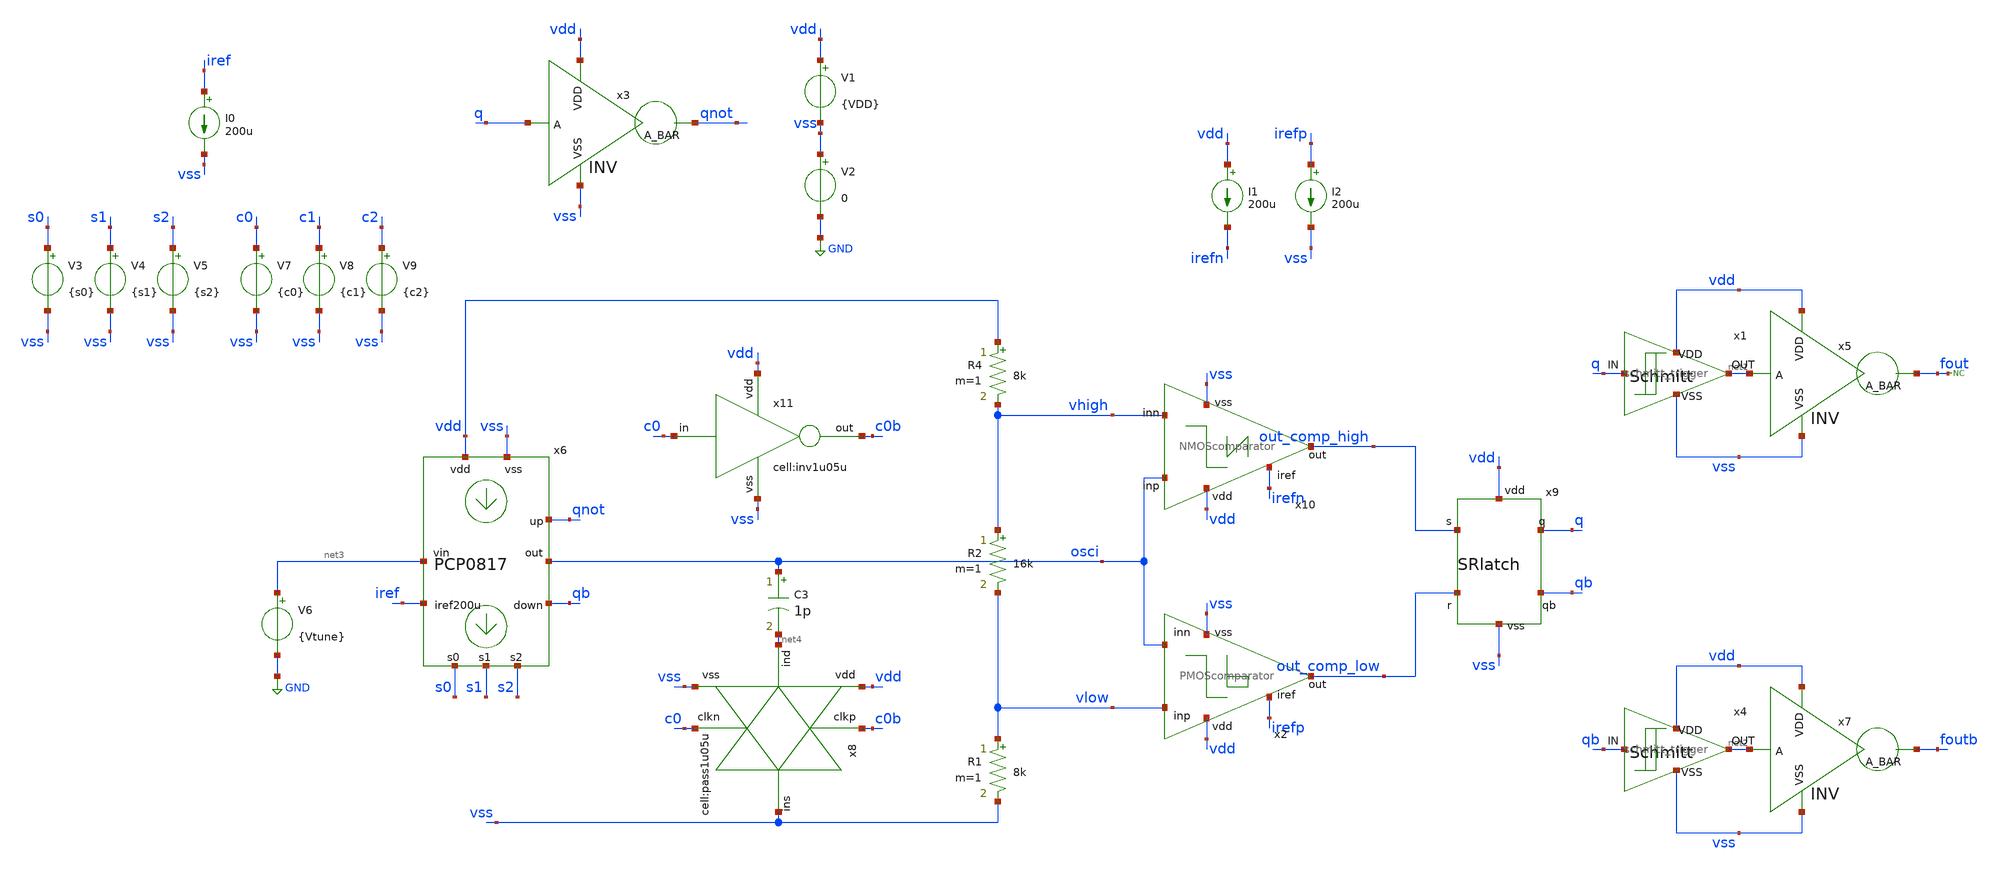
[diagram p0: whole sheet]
** sch_path: designs/libs/qw_core_analog_pkedit/VCO0818/VCO0818.sch
**.subckt VCO0818
V1 vdd vss {VDD}
V2 vss GND 0
I1 vdd irefn 200u
I2 irefp vss 200u
R1 vlow vss 8k m=1
R2 vhigh vlow 16k m=1
R4 vdd vhigh 8k m=1
x9 vdd out_comp_high q qb out_comp_low vss SRlatch
x2 vdd irefp vlow out_comp_low osci vss PMOScomparator
x10 vdd osci out_comp_high vhigh irefn vss NMOScomparator
x3 vdd q qnot vss INV
x1 q net1 vdd vss schmitt_trigger
x4 qb net2 vdd vss schmitt_trigger
x5 vdd net1 fout vss INV
x7 vdd net2 foutb vss INV
V6 net3 GND {Vtune}
I0 iref vss 200u
* noconn fout
x6 vdd vss net3 iref osci qnot qb s0 s1 s2 PCP0817
V3 s0 vss {s0}
V4 s1 vss {s1}
V5 s2 vss {s2}
V7 c0 vss {c0}
V8 c1 vss {c1}
V9 c2 vss {c2}
C3 osci net4 1p m=1
x8 net4 vss c0 vss c0b vdd pass1u05u
x11 c0 vdd c0b vss inv1u05u
**** begin user architecture code



.param VDD = 3.3
.param Vtune = 2.7
.param s0 = 3.3 s1 = 3.3 s2 = 3.3 c0 = 0 c1 = 0 c2 = 3.3
.param VIN=1
*V6 net3 0 {Vtune}
.meas tran period1 TRIG v(fout) VAL=1.65 RISE=15 TARG v(fout) VAL=1.65 RISE=16
.meas tran freq param='1/period1'

.control
save all

let vstart = 0.0
let vstop = 3.3
let vstep = 0.1

foreach VINVAL 2.1 2.2
    alterparam Vtune = $VINVAL
    reset
    tran 10p 100n
end

write VCO0818.raw
.endc



.include $::180MCU_MODELS/design.ngspice
.lib $::180MCU_MODELS/sm141064.ngspice typical
.lib $::180MCU_MODELS/sm141064.ngspice cap_mim
.lib $::180MCU_MODELS/sm141064.ngspice res_typical
.lib $::180MCU_MODELS/sm141064.ngspice moscap_typical
.lib $::180MCU_MODELS/sm141064.ngspice mimcap_typical
* .lib $::180MCU_MODELS/sm141064.ngspice res_statistical

**** end user architecture code
**.ends
.GLOBAL GND
.end
